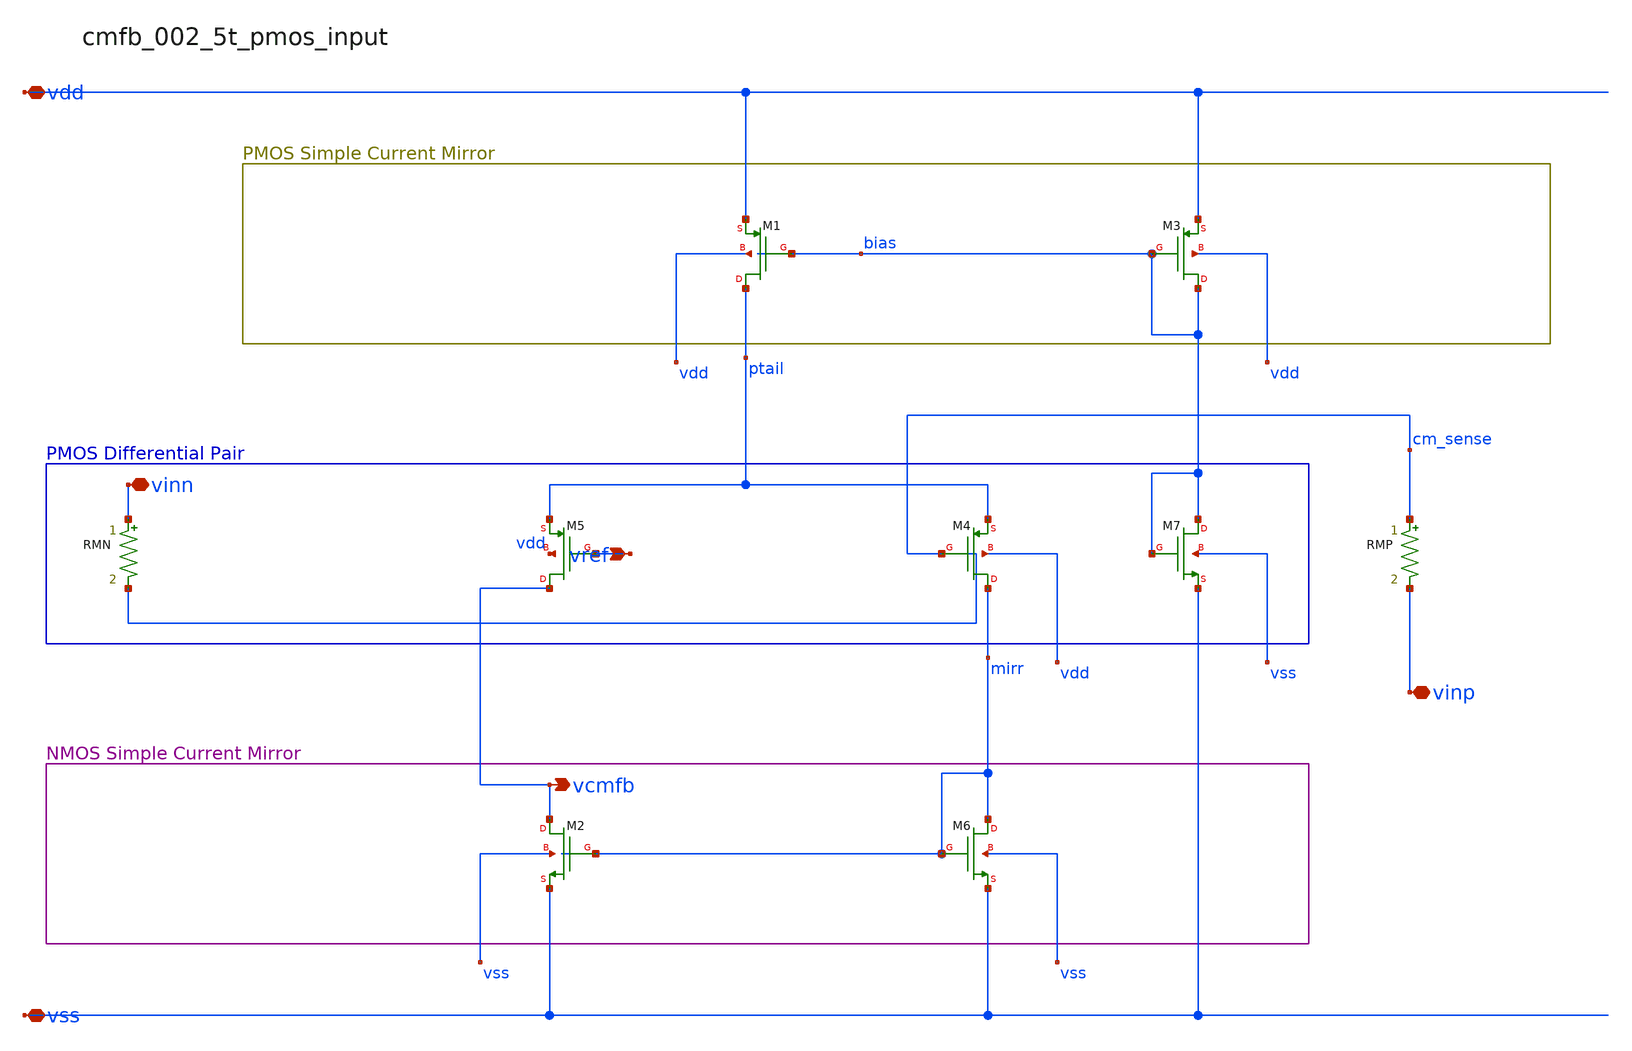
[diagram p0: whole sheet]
** sch_path: analog-db/raw/cmfb_002_5t_pmos_input/cmfb_002_5t_pmos_input_annotated.sch
**.subckt cmfb_002_5t_pmos_input_annotated vref vdd vinn vss vinp vcmfb
*.ipin vref
*.iopin vdd
*.iopin vinn
*.iopin vss
*.iopin vinp
*.opin vcmfb
RMN vinn cm_sense 'x_dut_rmn_value' m=1
RMP cm_sense vinp 'x_dut_rmp_value' m=1
XM1 ptail bias vdd vdd sg13_lv_pmos w=x_dut_xm1_w l=x_dut_xm1_l ng=1 m=x_dut_xm1_m
XM2 vcmfb mirr vss vss sg13_lv_nmos w=x_dut_xm2_w l=x_dut_xm2_l ng=1 m=x_dut_xm2_m
XM3 bias bias vdd vdd sg13_lv_pmos w=x_dut_xm3_w l=x_dut_xm3_l ng=1 m=x_dut_xm3_m
XM4 mirr cm_sense ptail vdd sg13_lv_pmos w=x_dut_xm4_w l=x_dut_xm4_l ng=1 m=x_dut_xm4_m
XM5 vcmfb vref ptail vdd sg13_lv_pmos w=x_dut_xm5_w l=x_dut_xm5_l ng=1 m=x_dut_xm5_m
XM6 mirr mirr vss vss sg13_lv_nmos w=x_dut_xm6_w l=x_dut_xm6_l ng=1 m=x_dut_xm6_m
XM7 bias bias vss vss sg13_lv_nmos w=x_dut_xm7_w l=x_dut_xm7_l ng=1 m=x_dut_xm7_m
**.ends
.end
